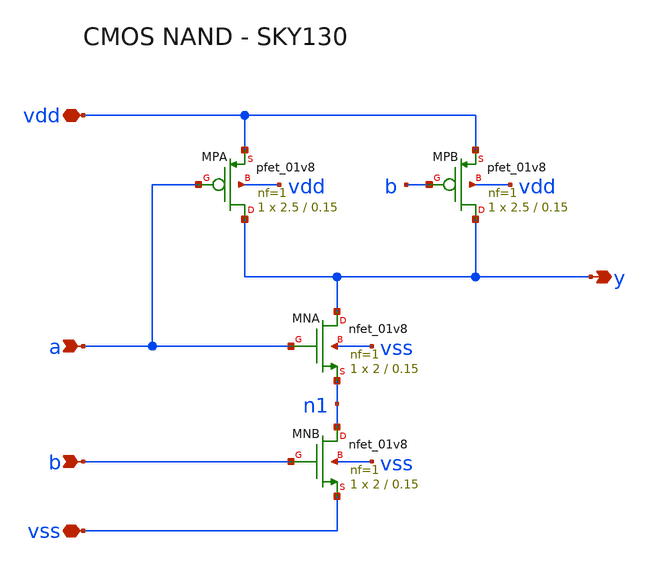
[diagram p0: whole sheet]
** sch_path: lab4/xschem/nand.sch
**.subckt nand a b y vdd vss
*.ipin a
*.ipin b
*.opin y
*.iopin vdd
*.iopin vss
XMPA y a vdd vdd sky130_fd_pr__pfet_01v8 L=0.15 W=2.5 nf=1 ad='int((nf+1)/2) * W/nf * 0.29' as='int((nf+2)/2) * W/nf * 0.29'
+ pd='2*int((nf+1)/2) * (W/nf + 0.29)' ps='2*int((nf+2)/2) * (W/nf + 0.29)' nrd='0.29 / W' nrs='0.29 / W'
+ sa=0 sb=0 sd=0 mult=1 m=1
XMPB y b vdd vdd sky130_fd_pr__pfet_01v8 L=0.15 W=2.5 nf=1 ad='int((nf+1)/2) * W/nf * 0.29' as='int((nf+2)/2) * W/nf * 0.29'
+ pd='2*int((nf+1)/2) * (W/nf + 0.29)' ps='2*int((nf+2)/2) * (W/nf + 0.29)' nrd='0.29 / W' nrs='0.29 / W'
+ sa=0 sb=0 sd=0 mult=1 m=1
XMNA y a n1 vss sky130_fd_pr__nfet_01v8 L=0.15 W=2 nf=1 ad='int((1 + 1)/2) * 2 / 1 * 0.29' as='int((1 + 2)/2) * 2 / 1 * 0.29'
+ pd='2*int((1 + 1)/2) * (2 / 1 + 0.29)' ps='2*int((1 + 2)/2) * (2 / 1 + 0.29)' nrd='0.29 / 2 ' nrs='0.29 / 2 '
+ sa=0 sb=0 sd=0 mult=1 m=1
XMNB n1 b vss vss sky130_fd_pr__nfet_01v8 L=0.15 W=2 nf=1 ad='int((1 + 1)/2) * 2 / 1 * 0.29' as='int((1 + 2)/2) * 2 / 1 * 0.29'
+ pd='2*int((1 + 1)/2) * (2 / 1 + 0.29)' ps='2*int((1 + 2)/2) * (2 / 1 + 0.29)' nrd='0.29 / 2 ' nrs='0.29 / 2 '
+ sa=0 sb=0 sd=0 mult=1 m=1
**.ends
.end
